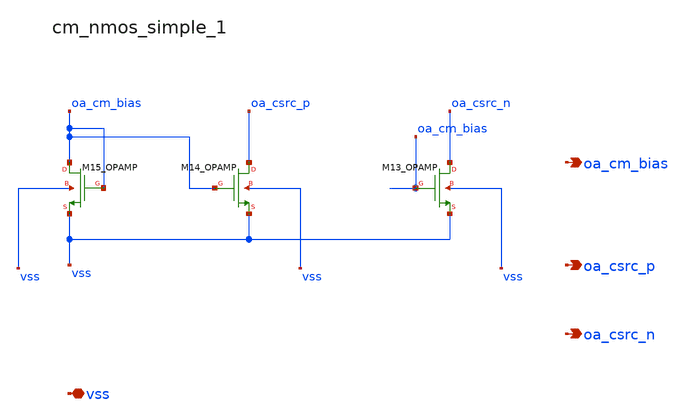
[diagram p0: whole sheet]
** sch_path: analog-db/raw/sup_003_rrl_sc_integrator/hier/blocks/cm_nmos_simple_1.sch
**.subckt cm_nmos_simple_1 vss oa_cm_bias oa_csrc_p oa_csrc_n
*.iopin vss
*.opin oa_cm_bias
*.opin oa_csrc_p
*.opin oa_csrc_n
XM13_OPAMP oa_csrc_n oa_cm_bias vss vss sg13_lv_nmos w=x_dut_xm13_opamp_w l=x_dut_xm13_opamp_l ng=1
+ m=x_dut_xm13_opamp_m
XM14_OPAMP oa_csrc_p oa_cm_bias vss vss sg13_lv_nmos w=x_dut_xm14_opamp_w l=x_dut_xm14_opamp_l ng=1
+ m=x_dut_xm14_opamp_m
XM15_OPAMP oa_cm_bias oa_cm_bias vss vss sg13_lv_nmos w=x_dut_xm15_opamp_w l=x_dut_xm15_opamp_l ng=1
+ m=x_dut_xm15_opamp_m
**.ends
.end
